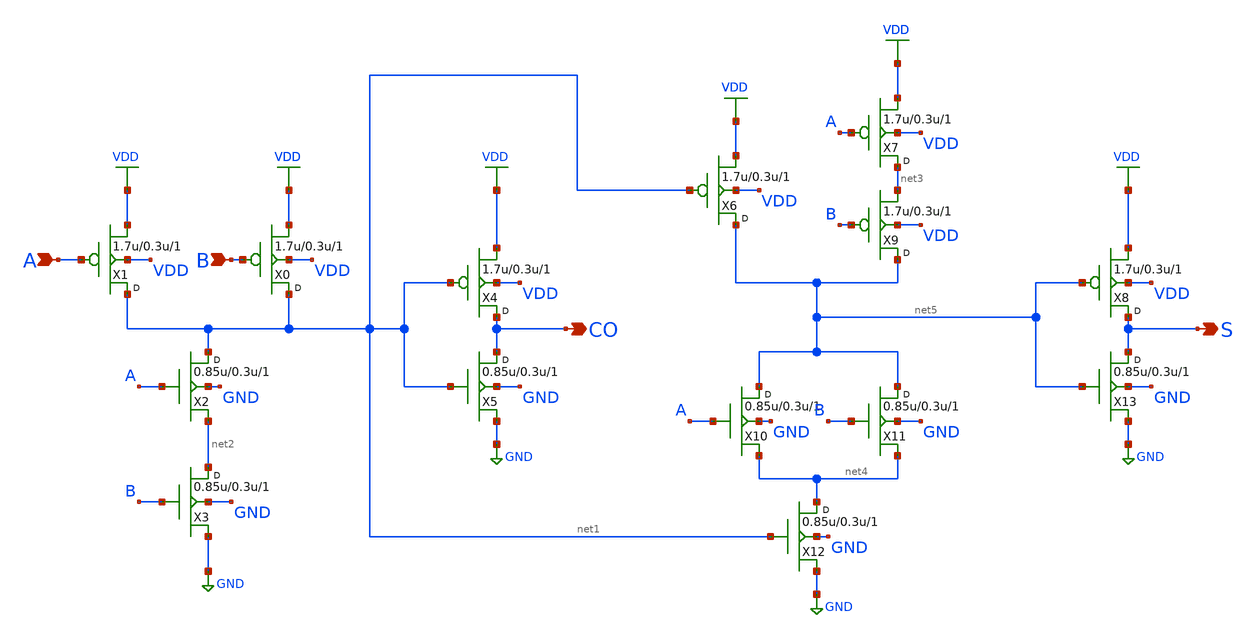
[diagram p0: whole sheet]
** sch_path: gf180mcu_osu_sc_gp12t3v3/cells/addh/gf180mcu_osu_sc_gp12t3v3__addh_1.sch
**.subckt gf180mcu_osu_sc_gp12t3v3__addh_1 A B CO S
*.ipin A
*.ipin B
*.opin CO
*.opin S
X1 net1 A VDD VDD pfet_03p3 w=1.7u l=0.3u m=1
X0 net1 B VDD VDD pfet_03p3 w=1.7u l=0.3u m=1
X2 net1 A net2 GND nfet_03p3 w=0.85u l=0.3u m=1
X3 net2 B GND GND nfet_03p3 w=0.85u l=0.3u m=1
X4 CO net1 VDD VDD pfet_03p3 w=1.7u l=0.3u m=1
X5 CO net1 GND GND nfet_03p3 w=0.85u l=0.3u m=1
X6 net5 net1 VDD VDD pfet_03p3 w=1.7u l=0.3u m=1
X7 net3 A VDD VDD pfet_03p3 w=1.7u l=0.3u m=1
X9 net5 B net3 VDD pfet_03p3 w=1.7u l=0.3u m=1
X10 net5 A net4 GND nfet_03p3 w=0.85u l=0.3u m=1
X11 net5 B net4 GND nfet_03p3 w=0.85u l=0.3u m=1
X12 net4 net1 GND GND nfet_03p3 w=0.85u l=0.3u m=1
X8 S net5 VDD VDD pfet_03p3 w=1.7u l=0.3u m=1
X13 S net5 GND GND nfet_03p3 w=0.85u l=0.3u m=1
**.ends
.GLOBAL VDD
.GLOBAL GND
.end
